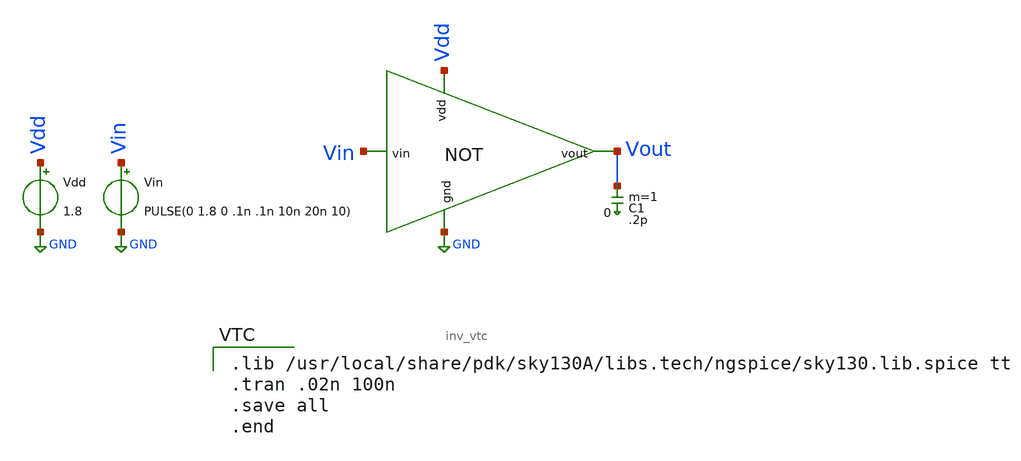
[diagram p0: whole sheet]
** sch_path: schematic/inv_test.sch
**.subckt inv_test
x1 Vdd Vout Vin GND inv_vtc
Vdd Vdd GND 1.8
Vin Vin GND PULSE(0 1.8 0 .1n .1n 10n 20n 10)
C1 Vout 0 .2p m=1
**** begin user architecture code

.lib /usr/local/share/pdk/sky130A/libs.tech/ngspice/sky130.lib.spice tt
.tran .02n 100n
.save all
.end

**** end user architecture code
**.ends

* expanding   symbol:  /home/subramanian/VLSI projects/schematic/inv_vtc.sym # of pins=4
** sym_path: schematic/inv_vtc.sym
** sch_path: schematic/inv_vtc.sch
.subckt inv_vtc vdd vout vin gnd
*.ipin vin
*.ipin vdd
*.opin vout
*.ipin gnd
XM1 vout vin gnd gnd sky130_fd_pr__nfet_01v8 L=0.15 W=1 nf=1 ad='int((1 + 1)/2) * 1 / 1 * 0.29' as='int((1 + 2)/2) * 1 / 1 * 0.29'
+ pd='2*int((1 + 1)/2) * (1 / 1 + 0.29)' ps='2*int((1 + 2)/2) * (1 / 1 + 0.29)' nrd='0.29 / 1 ' nrs='0.29 / 1 '
+ sa=0 sb=0 sd=0 mult=1 m=1
XM2 vout vin vdd vdd sky130_fd_pr__pfet_01v8 L=0.15 W=2 nf=1 ad='int((1 + 1)/2) * 2 / 1 * 0.29' as='int((1 + 2)/2) * 2 / 1 * 0.29'
+ pd='2*int((1 + 1)/2) * (2 / 1 + 0.29)' ps='2*int((1 + 2)/2) * (2 / 1 + 0.29)' nrd='0.29 / 2 ' nrs='0.29 / 2 '
+ sa=0 sb=0 sd=0 mult=1 m=1
.ends

.GLOBAL GND
.end
